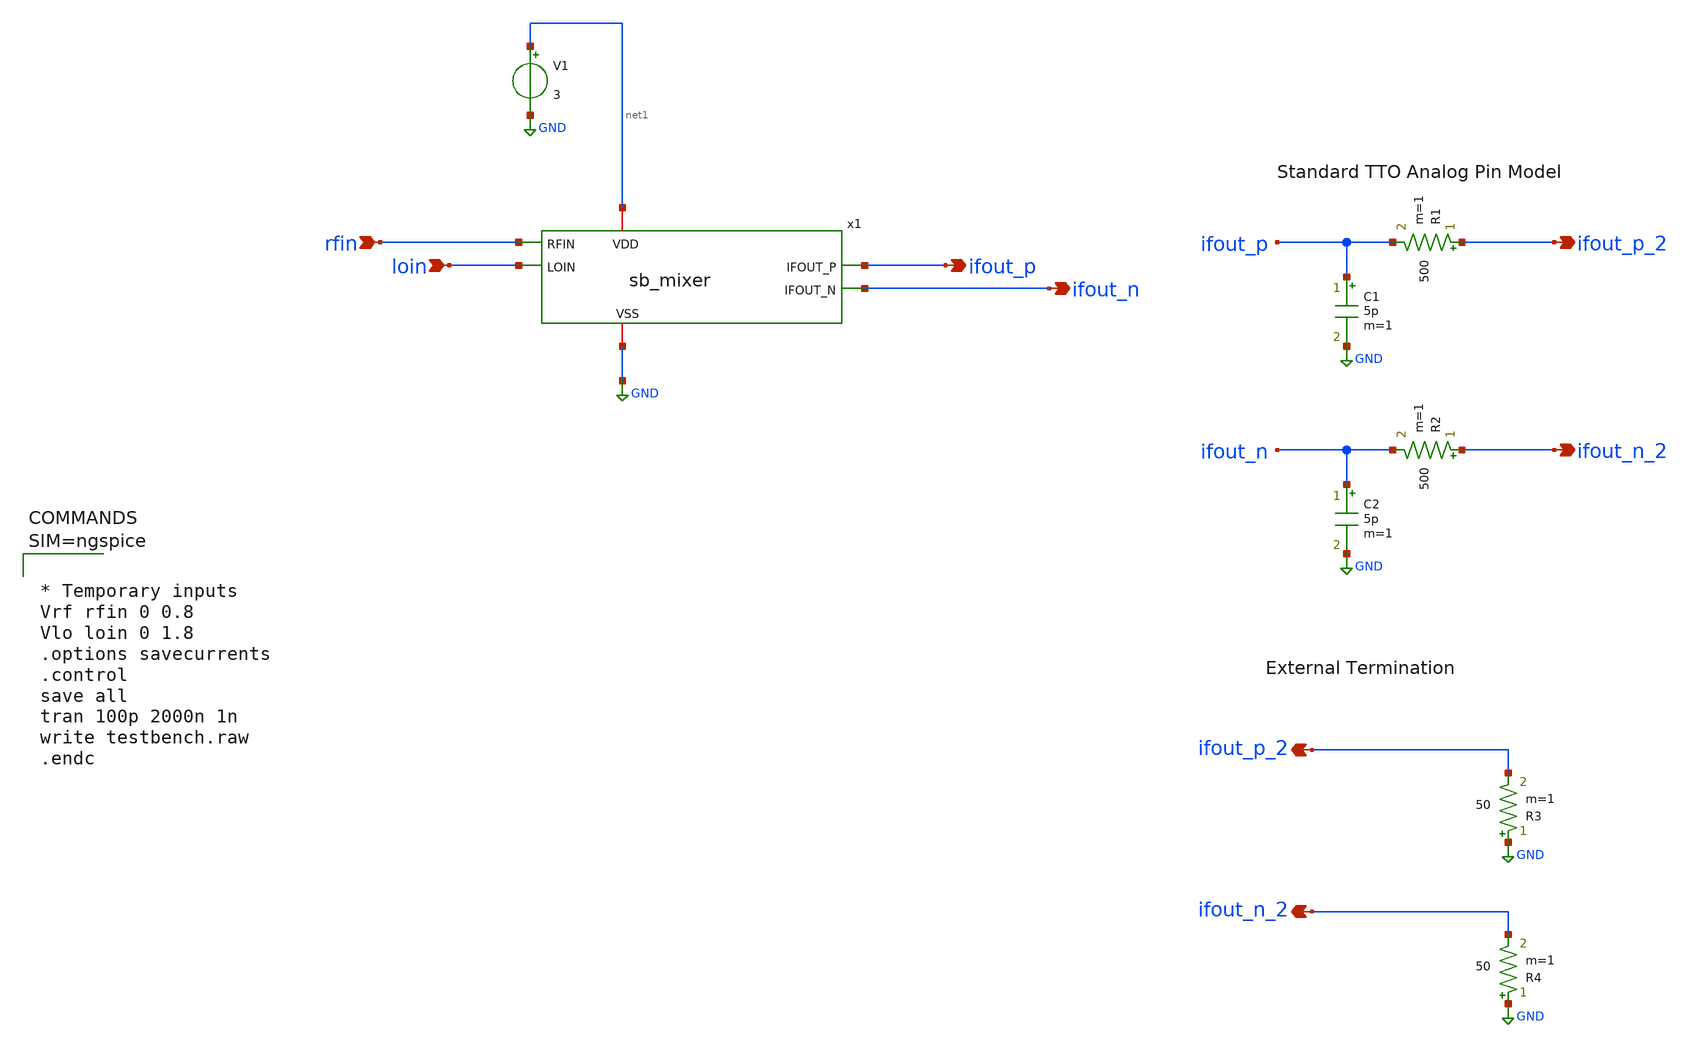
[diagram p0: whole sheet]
** sch_path: xschem/testbench.sch
**.subckt testbench loin rfin ifout_p ifout_n ifout_p_2 ifout_n_2 ifout_p_2 ifout_n_2
*.ipin loin
*.ipin rfin
*.opin ifout_p
*.opin ifout_n
*.opin ifout_p_2
*.opin ifout_n_2
*.opin ifout_p_2
*.opin ifout_n_2
x1 ifout_p ifout_n rfin net1 GND loin sb_mixer
V1 net1 GND 3
C1 ifout_p GND 5p m=1
R1 ifout_p_2 ifout_p 500 m=1
C2 ifout_n GND 5p m=1
R2 ifout_n_2 ifout_n 500 m=1
R3 GND ifout_p_2 50 m=1
R4 GND ifout_n_2 50 m=1
**** begin user architecture code

** opencircuitdesign pdks install
.lib $::SKYWATER_MODELS/sky130.lib.spice tt
.include $::SKYWATER_STDCELLS/sky130_fd_sc_hd.spice





* Temporary inputs
Vrf rfin 0 0.8
Vlo loin 0 1.8
.options savecurrents
.control
save all
tran 100p 2000n 1n
write testbench.raw
.endc



**** end user architecture code
**.ends

* expanding   symbol:  sb_mixer.sym # of pins=6
** sym_path: xschem/sb_mixer.sym
** sch_path: xschem/sb_mixer.sch
.subckt sb_mixer IFOUT_P IFOUT_N RFIN VDD VSS LOIN
*.iopin VDD
*.iopin VSS
*.ipin LOIN
*.ipin RFIN
*.opin IFOUT_P
*.opin IFOUT_N
x1 LOIN VSS VSS VDD VDD LO_N sky130_fd_sc_hd__inv_1
x2 LO_N VSS VSS VDD VDD LO_P sky130_fd_sc_hd__inv_1
XM1 net1 RFIN VSS VSS sky130_fd_pr__nfet_01v8_lvt L=2 W=10 nf=1 ad='int((nf+1)/2) * W/nf * 0.29' as='int((nf+2)/2) * W/nf * 0.29'
+ pd='2*int((nf+1)/2) * (W/nf + 0.29)' ps='2*int((nf+2)/2) * (W/nf + 0.29)' nrd='0.29 / W' nrs='0.29 / W'
+ sa=0 sb=0 sd=0 mult=1 m=1
XM2 IFOUT_P LO_P net1 VSS sky130_fd_pr__nfet_01v8 L=2 W=10 nf=1 ad='int((nf+1)/2) * W/nf * 0.29' as='int((nf+2)/2) * W/nf * 0.29'
+ pd='2*int((nf+1)/2) * (W/nf + 0.29)' ps='2*int((nf+2)/2) * (W/nf + 0.29)' nrd='0.29 / W' nrs='0.29 / W'
+ sa=0 sb=0 sd=0 mult=1 m=1
XM3 IFOUT_N LO_N net1 VSS sky130_fd_pr__nfet_01v8 L=2 W=10 nf=1 ad='int((nf+1)/2) * W/nf * 0.29' as='int((nf+2)/2) * W/nf * 0.29'
+ pd='2*int((nf+1)/2) * (W/nf + 0.29)' ps='2*int((nf+2)/2) * (W/nf + 0.29)' nrd='0.29 / W' nrs='0.29 / W'
+ sa=0 sb=0 sd=0 mult=1 m=1
XR1 IFOUT_P net2 VSS sky130_fd_pr__res_high_po_0p69 L=0.69 mult=1 m=1
XR2 IFOUT_N net2 VSS sky130_fd_pr__res_high_po_0p69 L=0.69 mult=1 m=1
.ends

.GLOBAL GND
.end
